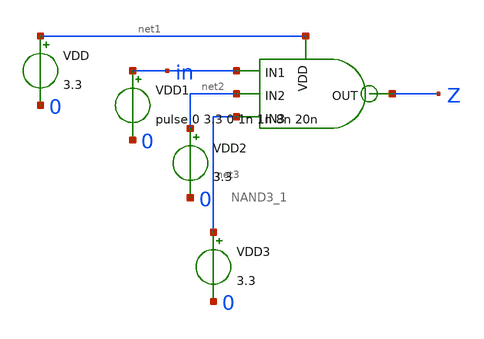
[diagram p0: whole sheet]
** sch_path: chipathon_2023/initial_notebooks_2023/accepted_notebooks/Current-Steering-DAC/DAC/Test_NAND3_1.sch
**.subckt Test_NAND3_1
VDD net1 0 3.3
VDD1 in 0 pulse 0 3.3 0 1n 1n 8n 20n
VDD2 net2 0 3.3
VDD3 net3 0 3.3
x1 net1 Z in net2 net3 NAND3_1
**** begin user architecture code




.include /foss/pdks/gf180mcuC/libs.tech/ngspice/design.ngspice
.lib /foss/pdks/gf180mcuC/libs.tech/ngspice/sm141064.ngspice typical


.control
	tran 0.1n 50n
	*dc vin1 0 3.3 0.1
	plot v(in) v(Z)
	*plot v(vout)
.endc
.save all




**** end user architecture code
**.ends
.end
